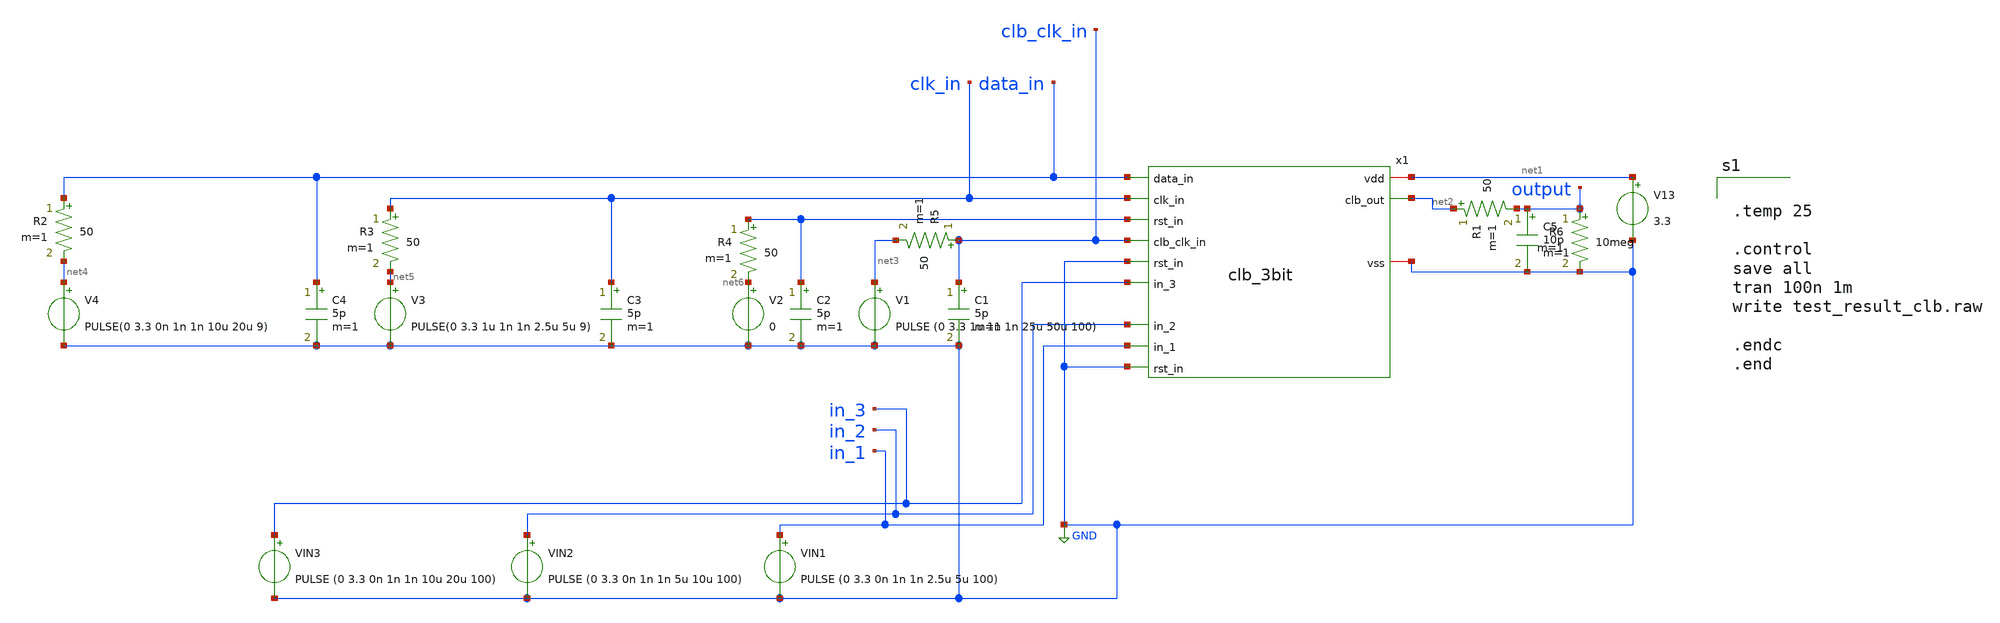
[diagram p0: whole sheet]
** sch_path: designs/digital/clb_mosbius/clb_3bit_tb.sch
**.subckt clb_3bit_tb
C1 clb_clk_in GND 5p m=1
C2 GND GND 5p m=1
C3 clk_in GND 5p m=1
C4 data_in GND 5p m=1
V1 net3 GND PULSE (0 3.3 1u 1n 1n 25u 50u 100)
V2 net6 GND 0
V3 net5 GND PULSE(0 3.3 1u 1n 1n 2.5u 5u 9)
V4 net4 GND PULSE(0 3.3 0n 1n 1n 10u 20u 9)
V13 net1 GND 3.3
C5 output GND 10p m=1
R1 net2 output 50 m=1
R2 data_in net4 50 m=1
R3 clk_in net5 50 m=1
R4 GND net6 50 m=1
R5 clb_clk_in net3 50 m=1
x1 data_in clk_in net1 GND net2 clb_clk_in in_3 in_2 in_1 GND clb_3bit
R6 output GND 10meg m=1
VIN1 in_1 GND PULSE (0 3.3 0n 1n 1n 2.5u 5u 100)
VIN2 in_2 GND PULSE (0 3.3 0n 1n 1n 5u 10u 100)
VIN3 in_3 GND PULSE (0 3.3 0n 1n 1n 10u 20u 100)
**** begin user architecture code

.include /home/raditya/Silicons/pdks/gf180mcuD/libs.tech/ngspice/design.ngspice
.lib /home/raditya/Silicons/pdks/gf180mcuD/libs.tech/ngspice/sm141064.ngspice ff



.temp 25

.control
save all
tran 100n 1m
write test_result_clb.raw

.endc
.end


**** end user architecture code
**.ends
.GLOBAL GND
.end
